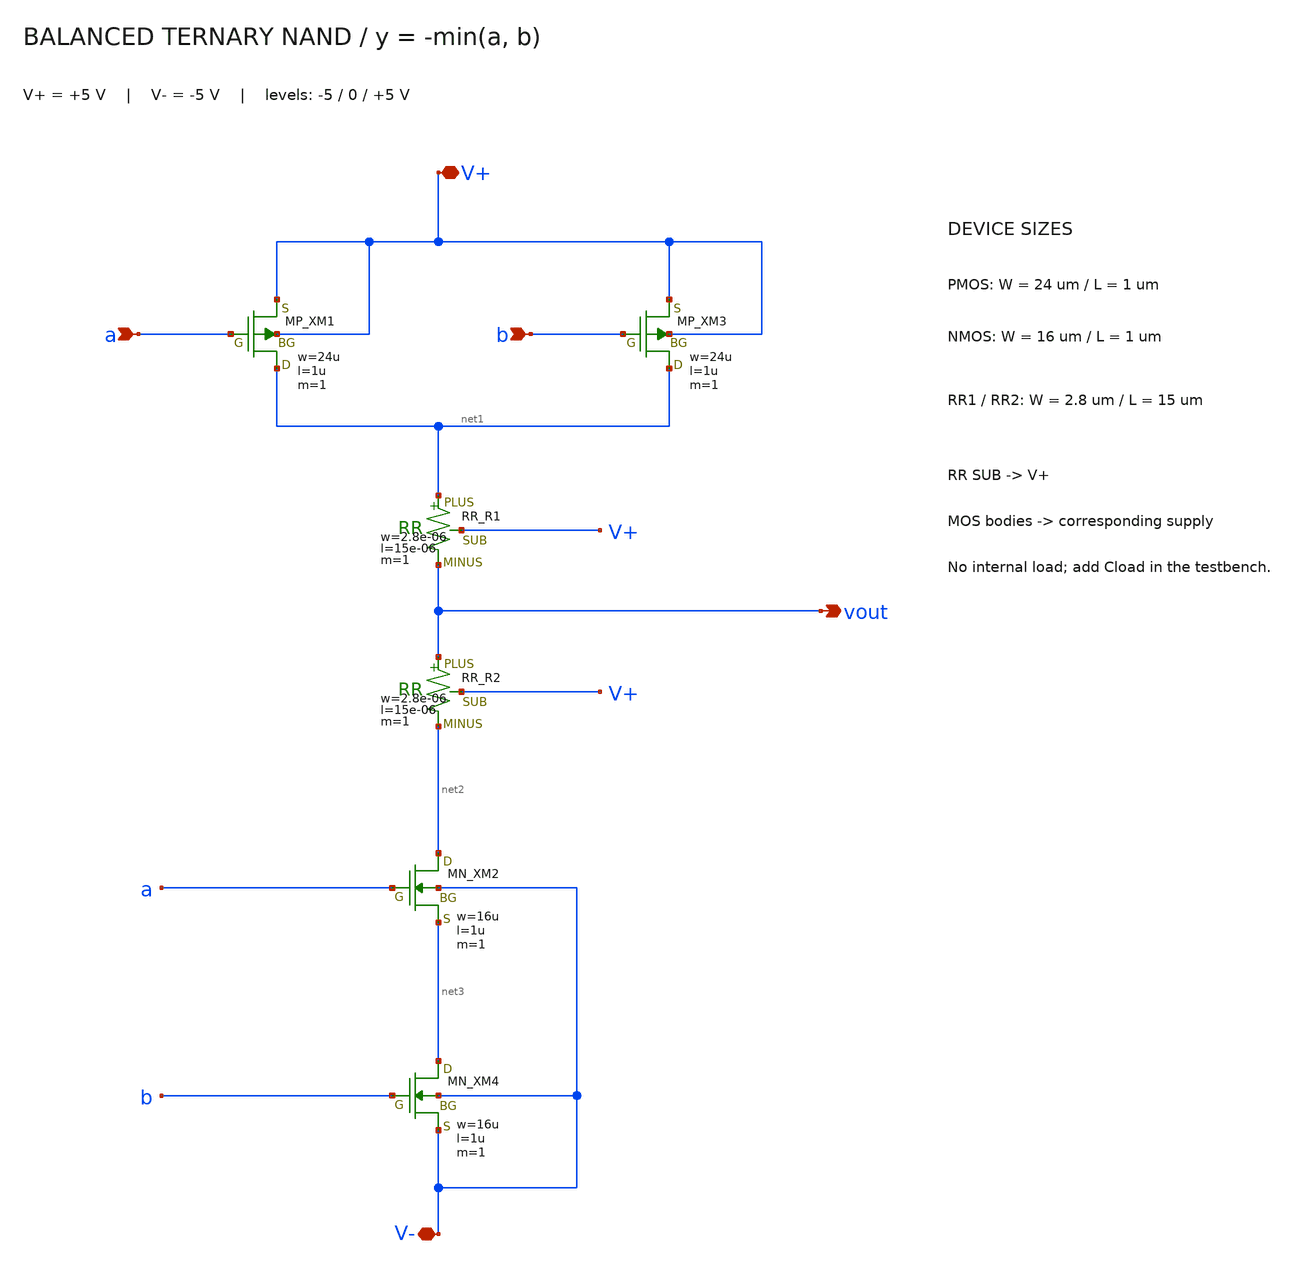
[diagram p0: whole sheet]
** sch_path: member_project/balanced-ternary-logic/PenguinEino/nand.sch
**.subckt nand V+ a b vout V-
*.iopin V+
*.ipin a
*.ipin b
*.opin vout
*.iopin V-
XXM1 net1 a V+ V+ PMOS w=24u l=1u nrd=0 nrs=0 m=1
XXM3 net1 b V+ V+ PMOS w=24u l=1u nrd=0 nrs=0 m=1
XR1 net1 vout V+ F_RR w=2.8e-06 l=15e-06 R=1 tc1=0 tc2=0 m=1
XR2 vout net2 V+ F_RR w=2.8e-06 l=15e-06 R=1 tc1=0 tc2=0 m=1
XXM2 net2 a net3 V- NMOS w=16u l=1u nrd=0 nrs=0 m=1
XXM4 net3 b V- V- NMOS w=16u l=1u nrd=0 nrs=0 m=1
**.ends
.end
